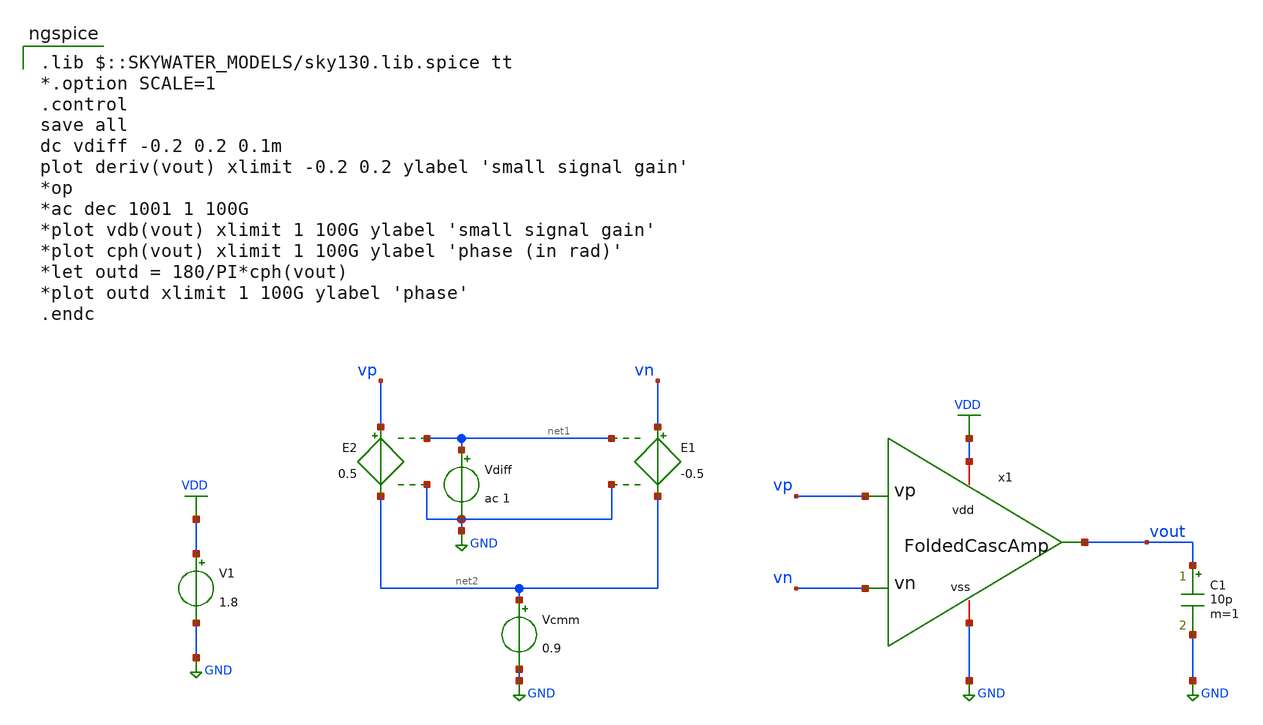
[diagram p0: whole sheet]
** sch_path: images/align/design/Examples/FoldedCascodeAmplifier/FoldedCascAmp_Tb.sch
**.subckt FoldedCascAmp_Tb
E1 vn net2 net1 GND -0.5
E2 vp net2 net1 GND 0.5
Vdiff net1 GND ac 1
V1 VDD GND 1.8
Vcmm net2 GND 0.9
C1 vout GND 10p m=1
x1 VDD vout vn vp GND FoldedCascAmp
**** begin user architecture code
 .lib $::SKYWATER_MODELS/sky130.lib.spice tt
*.option SCALE=1
.control
save all
dc vdiff -0.2 0.2 0.1m
plot deriv(vout) xlimit -0.2 0.2 ylabel 'small signal gain'
*op
*ac dec 1001 1 100G
*plot vdb(vout) xlimit 1 100G ylabel 'small signal gain'
*plot cph(vout) xlimit 1 100G ylabel 'phase (in rad)'
*let outd = 180/PI*cph(vout)
*plot outd xlimit 1 100G ylabel 'phase'
.endc
**** end user architecture code
**.ends
.GLOBAL GND
.GLOBAL VDD
.end
